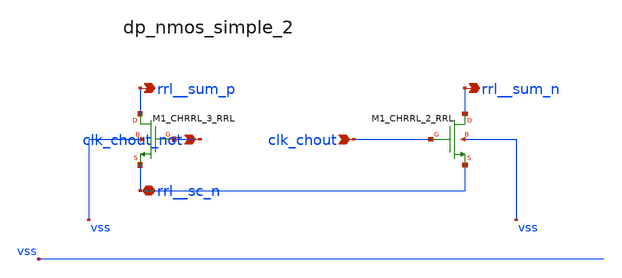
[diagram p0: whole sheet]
** sch_path: analog-db/raw/ia_004_fan_chopper_rrl/hier/blocks/dp_nmos_simple_2.sch
**.subckt dp_nmos_simple_2 clk_chout_not clk_chout rrl__sc_n rrl__sum_p rrl__sum_n
*.ipin clk_chout_not
*.ipin clk_chout
*.iopin rrl__sc_n
*.opin rrl__sum_p
*.opin rrl__sum_n
XM1_CHRRL_2_RRL rrl__sum_n clk_chout rrl__sc_n vss sg13_lv_nmos w=x_dut_xm1_chrrl_2_rrl_w
+ l=x_dut_xm1_chrrl_2_rrl_l ng=1 m=x_dut_xm1_chrrl_2_rrl_m
XM1_CHRRL_3_RRL rrl__sum_p clk_chout_not rrl__sc_n vss sg13_lv_nmos w=x_dut_xm1_chrrl_3_rrl_w
+ l=x_dut_xm1_chrrl_3_rrl_l ng=1 m=x_dut_xm1_chrrl_3_rrl_m
**.ends
.end
